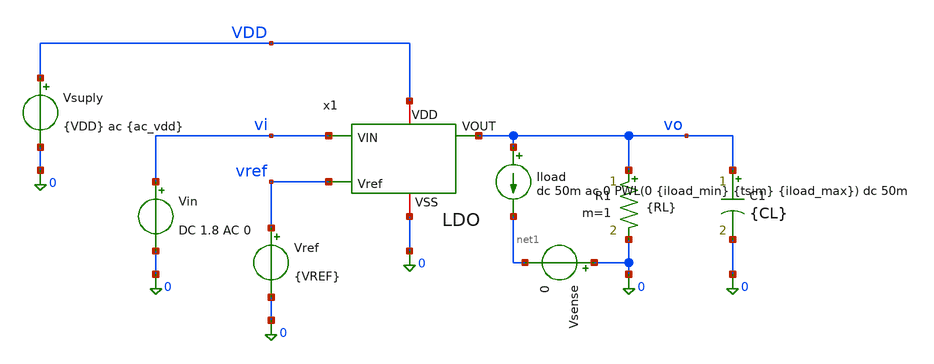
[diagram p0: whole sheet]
** sch_path: xschem/ldo_tb_psrr_loadregulation.sch
**.subckt ldo_tb_psrr_loadregulation
x1 vi vo VDD vref 0 LDO
Vsuply VDD 0 {VDD} ac {ac_vdd}
Vref vref 0 {VREF}
Vin vi 0 DC 1.8 AC 0
R1 vo 0 {RL} m=1
C1 vo 0 {CL} m=1
Iload vo net1 dc 50m ac 0 PWL(0 {iload_min} {tsim} {iload_max}) dc 50m
Vsense 0 net1 0
**** begin user architecture code




* 1. Inclusión de libreria de modelos Sky130 PRIMERO
.lib /foss/pdks/sky130A/libs.tech/ngspice/sky130.lib.spice ss

**parametros_ldo

.param ac_iprobe = 0
.param ac_vdd = 1

.param VDD = 1.8
.param VREF = 0.6
.param VIN = 1.8
.param RL = 999k
.param CL = 1u
.param tsim = 2m
* Parámetros para la prueba de carga del LDO
.param iload_min = 100u
.param iload_max = 50m
.param tstart   = 10u
.param trise    = 100n
.param tfall    = 100n
.param twidth   = 200u
.param tperiod  = 400u
.param tsim = '5*tperiod'

.control
let tperiod  = 400u
let tsim = '5*tperiod'


set filetype=ascii

* Punto de Operación (.OP)
op
write LDO_op.raw

* Análisis en dc sweep para el load regulation
dc iload 100u 50m 100u
*plot vo
*plot vsense#branch

* Analisis en dc sweep para el line regulation
dc vin 1.3 2 0.01
*plot vo
*plot vi

write LDO_trans.raw

*análisis en Frecuencia (.AC) para el PSRR
ac dec 10 1 1G
write LDO_ac.raw

* 1. Ganancia de Lazo Abierto T(s) = v(x1.vre) / v(x1.net3)
let psrr1 = v(vdd)/v(vo)
let psrr_db = vdb(psrr1)

* 5. Graficar la magnitud
*plot psrr_db


setplot ac1
meas ac ganancia_1   find psrr_db at=1
meas ac ganancia_1k  find psrr_db at=1k
meas ac ganancia_10k find psrr_db at=10k
meas ac ganancia_1M  find psrr_db at=1Meg


setplot dc1
meas dc voload_max MAX v(vo)
meas dc voload_min MIN v(vo)
let load_regulation = voload_max - voload_min
echo 'load_regulation = $&load_regulation'

setplot dc2
meas dc voline_max MAX v(vo)
meas dc voline_min MIN v(vo)
let line_regulation = voline_max - voline_min
echo 'line_regulation = $&line_regulation'

.endc



**** end user architecture code
**.ends

* expanding   symbol:  /foss/designs/LDO-sky130/xschem/LDO.sym # of pins=5
** sym_path: xschem/LDO.sym
** sch_path: xschem/LDO.sch
.subckt LDO VIN VOUT VDD Vref VSS
*.ipin VIN
*.iopin VDD
*.opin VOUT
*.ipin Vref
*.iopin VSS
x1 VDD net2 Vref net3 net1 VSS OTA
I0 VDD net1 10u
XM1 VOUT net2 VIN VDD sky130_fd_pr__pfet_01v8_lvt L=0.35 W=1000 nf=50 ad='int((50 + 1)/2) * 1000 / 50 * 0.29'
+ as='int((50 + 2)/2) * 1000 / 50 * 0.29' pd='2*int((50 + 1)/2) * (1000 / 50 + 0.29)' ps='2*int((50 + 2)/2) * (1000 / 50 + 0.29)'
+ nrd='0.29 / 1000 ' nrs='0.29 / 1000 ' sa=0 sb=0 sd=0 mult=5 m=5
XR1 Vre VOUT VDD sky130_fd_pr__res_iso_pw W=0.35 L=10 m=1
XR2 VSS Vre VDD sky130_fd_pr__res_iso_pw W=0.35 L=10 m=1
V1 net3 Vre 0 ac {ac_iprobe}
XC1 VOUT Vre sky130_fd_pr__cap_mim_m3_2 W=19.5 L=19.5 MF=1 m=1
.ends


* expanding   symbol:  /foss/designs/LDO-sky130/xschem/OTA.sym # of pins=6
** sym_path: xschem/OTA.sym
** sch_path: xschem/OTA.sch
.subckt OTA VDD VO_ota VIN_ota VIP_ota Iref VSS
*.ipin VIN_ota
*.opin VO_ota
*.iopin Iref
*.iopin VSS
*.iopin VDD
*.ipin VIP_ota
XMr Iref Iref VSS VSS sky130_fd_pr__nfet_01v8 L=0.5 W=0.5 nf=1 ad='int((1 + 1)/2) * 0.5 / 1 * 0.29' as='int((1 + 2)/2) * 0.5 / 1 * 0.29'
+ pd='2*int((1 + 1)/2) * (0.5 / 1 + 0.29)' ps='2*int((1 + 2)/2) * (0.5 / 1 + 0.29)' nrd='0.29 / 0.5 ' nrs='0.29 / 0.5 '
+ sa=0 sb=0 sd=0 mult=1 m=1
XMo VO_ota VO_ota1 VDD VDD sky130_fd_pr__pfet_01v8 L=0.5 W=20 nf=1 ad='int((1 + 1)/2) * 20 / 1 * 0.29'
+ as='int((1 + 2)/2) * 20 / 1 * 0.29' pd='2*int((1 + 1)/2) * (20 / 1 + 0.29)' ps='2*int((1 + 2)/2) * (20 / 1 + 0.29)'
+ nrd='0.29 / 20 ' nrs='0.29 / 20 ' sa=0 sb=0 sd=0 mult=1 m=1
XMrc1 Vtail Iref VSS VSS sky130_fd_pr__nfet_01v8 L=0.5 W=2 nf=1 ad='int((1 + 1)/2) * 2 / 1 * 0.29' as='int((1 + 2)/2) * 2 / 1 * 0.29'
+ pd='2*int((1 + 1)/2) * (2 / 1 + 0.29)' ps='2*int((1 + 2)/2) * (2 / 1 + 0.29)' nrd='0.29 / 2 ' nrs='0.29 / 2 '
+ sa=0 sb=0 sd=0 mult=1 m=1
XMc2 VO_ota Iref VSS VSS sky130_fd_pr__nfet_01v8 L=0.5 W=1 nf=1 ad='int((1 + 1)/2) * 1 / 1 * 0.29' as='int((1 + 2)/2) * 1 / 1 * 0.29'
+ pd='2*int((1 + 1)/2) * (1 / 1 + 0.29)' ps='2*int((1 + 2)/2) * (1 / 1 + 0.29)' nrd='0.29 / 1 ' nrs='0.29 / 1 '
+ sa=0 sb=0 sd=0 mult=1 m=1
XMn VGP VIN_ota Vtail VSS sky130_fd_pr__nfet_01v8 L=0.5 W=40 nf=1 ad='int((1 + 1)/2) * 40 / 1 * 0.29'
+ as='int((1 + 2)/2) * 40 / 1 * 0.29' pd='2*int((1 + 1)/2) * (40 / 1 + 0.29)' ps='2*int((1 + 2)/2) * (40 / 1 + 0.29)'
+ nrd='0.29 / 40 ' nrs='0.29 / 40 ' sa=0 sb=0 sd=0 mult=1 m=1
XMp VO_ota1 VIP_ota Vtail VSS sky130_fd_pr__nfet_01v8 L=0.5 W=40 nf=1 ad='int((1 + 1)/2) * 40 / 1 * 0.29'
+ as='int((1 + 2)/2) * 40 / 1 * 0.29' pd='2*int((1 + 1)/2) * (40 / 1 + 0.29)' ps='2*int((1 + 2)/2) * (40 / 1 + 0.29)'
+ nrd='0.29 / 40 ' nrs='0.29 / 40 ' sa=0 sb=0 sd=0 mult=1 m=1
XMpr VO_ota1 VGP VDD VDD sky130_fd_pr__pfet_01v8 L=0.5 W=40 nf=1 ad='int((1 + 1)/2) * 40 / 1 * 0.29'
+ as='int((1 + 2)/2) * 40 / 1 * 0.29' pd='2*int((1 + 1)/2) * (40 / 1 + 0.29)' ps='2*int((1 + 2)/2) * (40 / 1 + 0.29)'
+ nrd='0.29 / 40 ' nrs='0.29 / 40 ' sa=0 sb=0 sd=0 mult=1 m=1
XMnr VGP VGP VDD VDD sky130_fd_pr__pfet_01v8 L=0.5 W=40 nf=1 ad='int((1 + 1)/2) * 40 / 1 * 0.29' as='int((1 + 2)/2) * 40 / 1 * 0.29'
+ pd='2*int((1 + 1)/2) * (40 / 1 + 0.29)' ps='2*int((1 + 2)/2) * (40 / 1 + 0.29)' nrd='0.29 / 40 ' nrs='0.29 / 40 '
+ sa=0 sb=0 sd=0 mult=1 m=1
XR1 VO_ota1 net1 VDD sky130_fd_pr__res_high_po W=0.35 L=360 mult=1 m=1
XC1 VO_ota net1 sky130_fd_pr__cap_mim_m3_2 W=50 L=50 MF=1 m=1
.ends

.end
